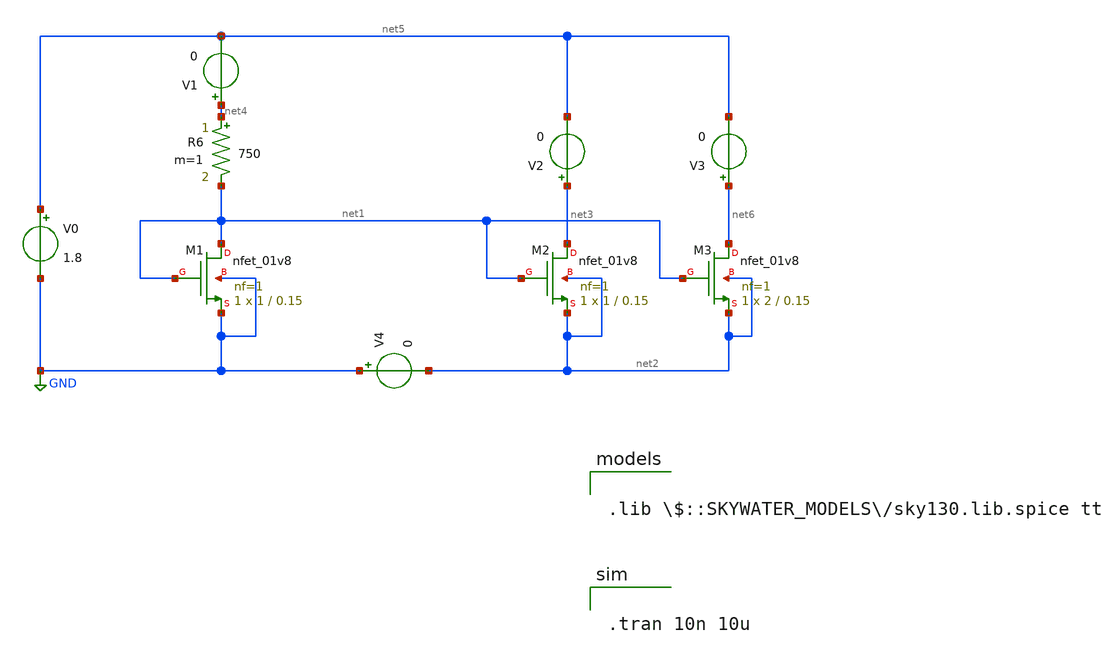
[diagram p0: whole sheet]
** sch_path: design/playground/current-mirror_1v8_tb.sch
**.subckt current-mirror_1v8_tb
R6 net4 net1 750 m=1
XM1 net1 net1 GND GND sky130_fd_pr__nfet_01v8 L=0.15 W=1 nf=1 ad='int((nf+1)/2) * W/nf * 0.29' as='int((nf+2)/2) * W/nf * 0.29'
+ pd='2*int((nf+1)/2) * (W/nf + 0.29)' ps='2*int((nf+2)/2) * (W/nf + 0.29)' nrd='0.29 / W' nrs='0.29 / W'
+ sa=0 sb=0 sd=0 mult=1 m=1
V0 net5 GND 1.8
XM2 net3 net1 net2 net2 sky130_fd_pr__nfet_01v8 L=0.15 W=1 nf=1 ad='int((nf+1)/2) * W/nf * 0.29' as='int((nf+2)/2) * W/nf * 0.29'
+ pd='2*int((nf+1)/2) * (W/nf + 0.29)' ps='2*int((nf+2)/2) * (W/nf + 0.29)' nrd='0.29 / W' nrs='0.29 / W'
+ sa=0 sb=0 sd=0 mult=1 m=1
V2 net3 net5 0
V1 net4 net5 0
XM3 net6 net1 net2 net2 sky130_fd_pr__nfet_01v8 L=0.15 W=2 nf=1 ad='int((nf+1)/2) * W/nf * 0.29' as='int((nf+2)/2) * W/nf * 0.29'
+ pd='2*int((nf+1)/2) * (W/nf + 0.29)' ps='2*int((nf+2)/2) * (W/nf + 0.29)' nrd='0.29 / W' nrs='0.29 / W'
+ sa=0 sb=0 sd=0 mult=1 m=1
V3 net6 net5 0
V4 GND net2 0
**** begin user architecture code


.tran 10n 10u



.lib $::SKYWATER_MODELS/sky130.lib.spice tt

**** end user architecture code
**.ends
.GLOBAL GND
.end
